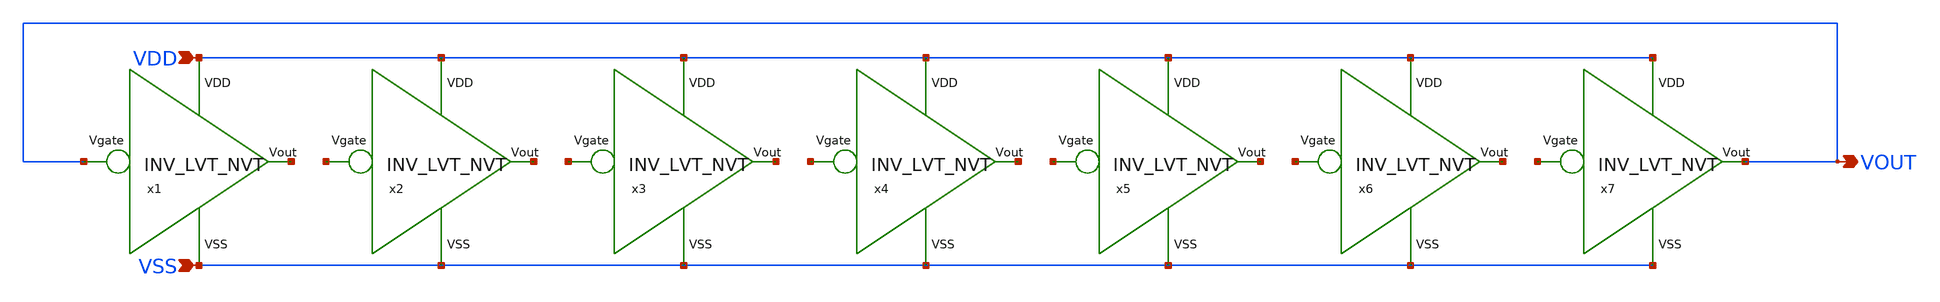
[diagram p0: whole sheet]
** sch_path: design/THESIS_EXP_RO_INVERTER_SKY130A/RO_LVT_NVT.sch
**.subckt RO_LVT_NVT VDD VSS VOUT
*.ipin VDD
*.ipin VSS
*.opin VOUT
x1 VDD VOUT net1 VSS INV_LVT_NVT
x2 VDD net2 net3 VSS INV_LVT_NVT
x3 VDD net4 net5 VSS INV_LVT_NVT
x4 VDD net6 net7 VSS INV_LVT_NVT
x5 VDD net8 net9 VSS INV_LVT_NVT
x6 VDD net10 net11 VSS INV_LVT_NVT
x7 VDD net12 VOUT VSS INV_LVT_NVT
**.ends
.end
